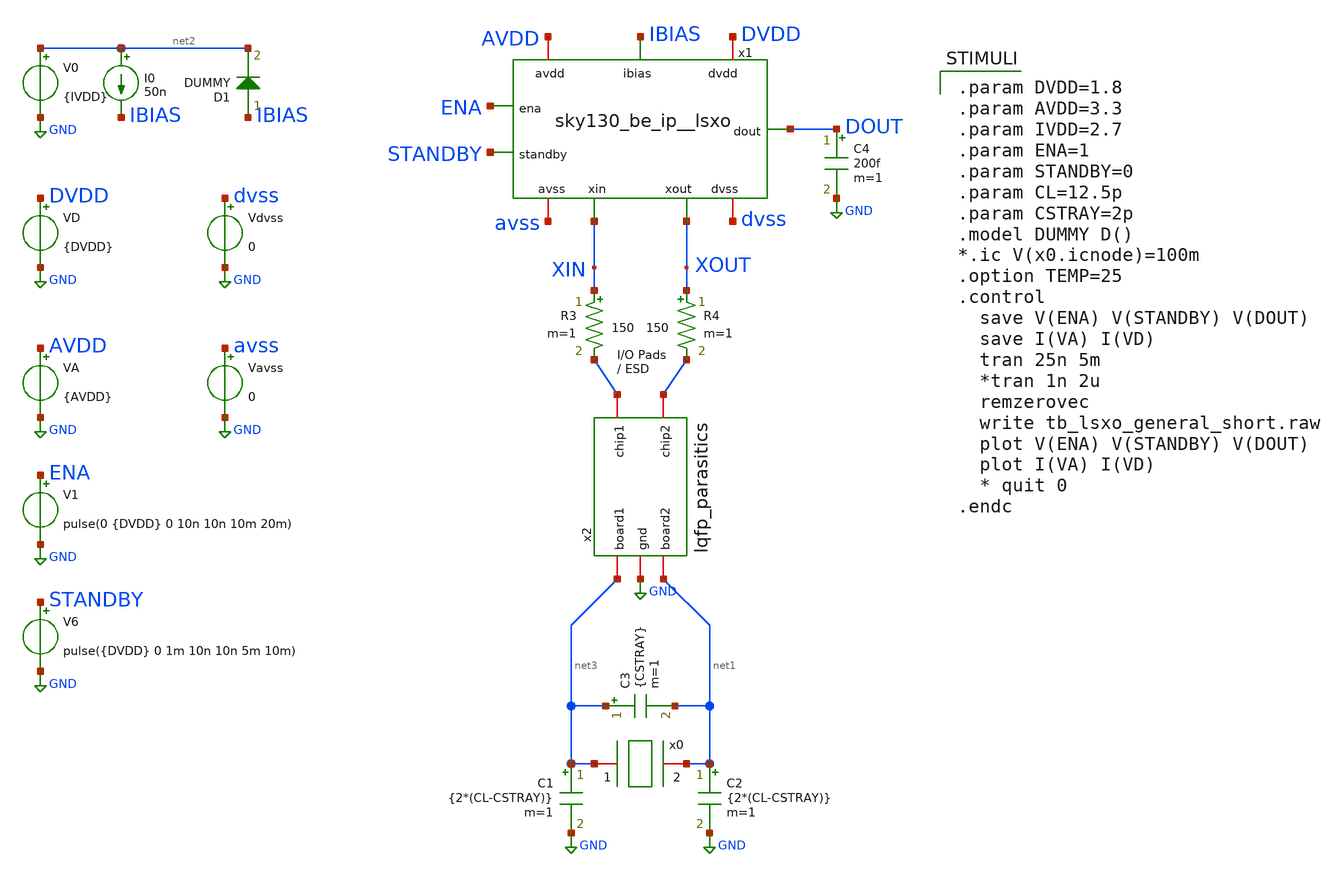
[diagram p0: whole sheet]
** sch_path: xschem/tb_man__sky130_be_ip__lsxo.sch

.lib $::SKYWATER_MODELS/sky130.lib.spice ff
.include $::SKYWATER_STDCELLS/sky130_fd_sc_hd.spice

**.subckt tb_man__sky130_be_ip__lsxo
VD DVDD GND {DVDD}
VA AVDD GND {AVDD}
C1 net3 GND {2*(CL-CSTRAY)} m=1
C2 net1 GND {2*(CL-CSTRAY)} m=1
C3 net3 net1 {CSTRAY} m=1
I0 net2 IBIAS 50n
C4 DOUT GND 200f m=1
V0 net2 GND {IVDD}
V6 STANDBY GND pulse({DVDD} 0 1m 10n 10n 5m 10m)
R3 XIN net4 150 m=1
R4 XOUT net5 150 m=1
x2 net5 net4 GND net3 net1 lqfp_parasitics
V1 ENA GND pulse(0 {DVDD} 0 10n 10n 10m 20m)
D1 IBIAS net2 DUMMY area=100
x1 AVDD avss DVDD dvss IBIAS ENA STANDBY DOUT XIN XOUT sky130_be_ip__lsxo
x0 net3 net1 xtal_iqd_125_1
Vdvss dvss GND 0
Vavss avss GND 0
**** begin user architecture code

.param DVDD=1.8
.param AVDD=3.3
.param IVDD=2.7
.param ENA=1
.param STANDBY=0
.param CL=12.5p
.param CSTRAY=2p
.model DUMMY D()
*.ic V(x0.icnode)=100m
.option TEMP=25
.control
  save V(ENA) V(STANDBY) V(DOUT)
  save I(VA) I(VD)
  tran 25n 5m
  *tran 1n 2u
  remzerovec
  write tb_lsxo_general_short.raw
  plot V(ENA) V(STANDBY) V(DOUT)
  plot I(VA) I(VD)
  * quit 0
.endc

**** end user architecture code
**.ends
.GLOBAL GND
.end
